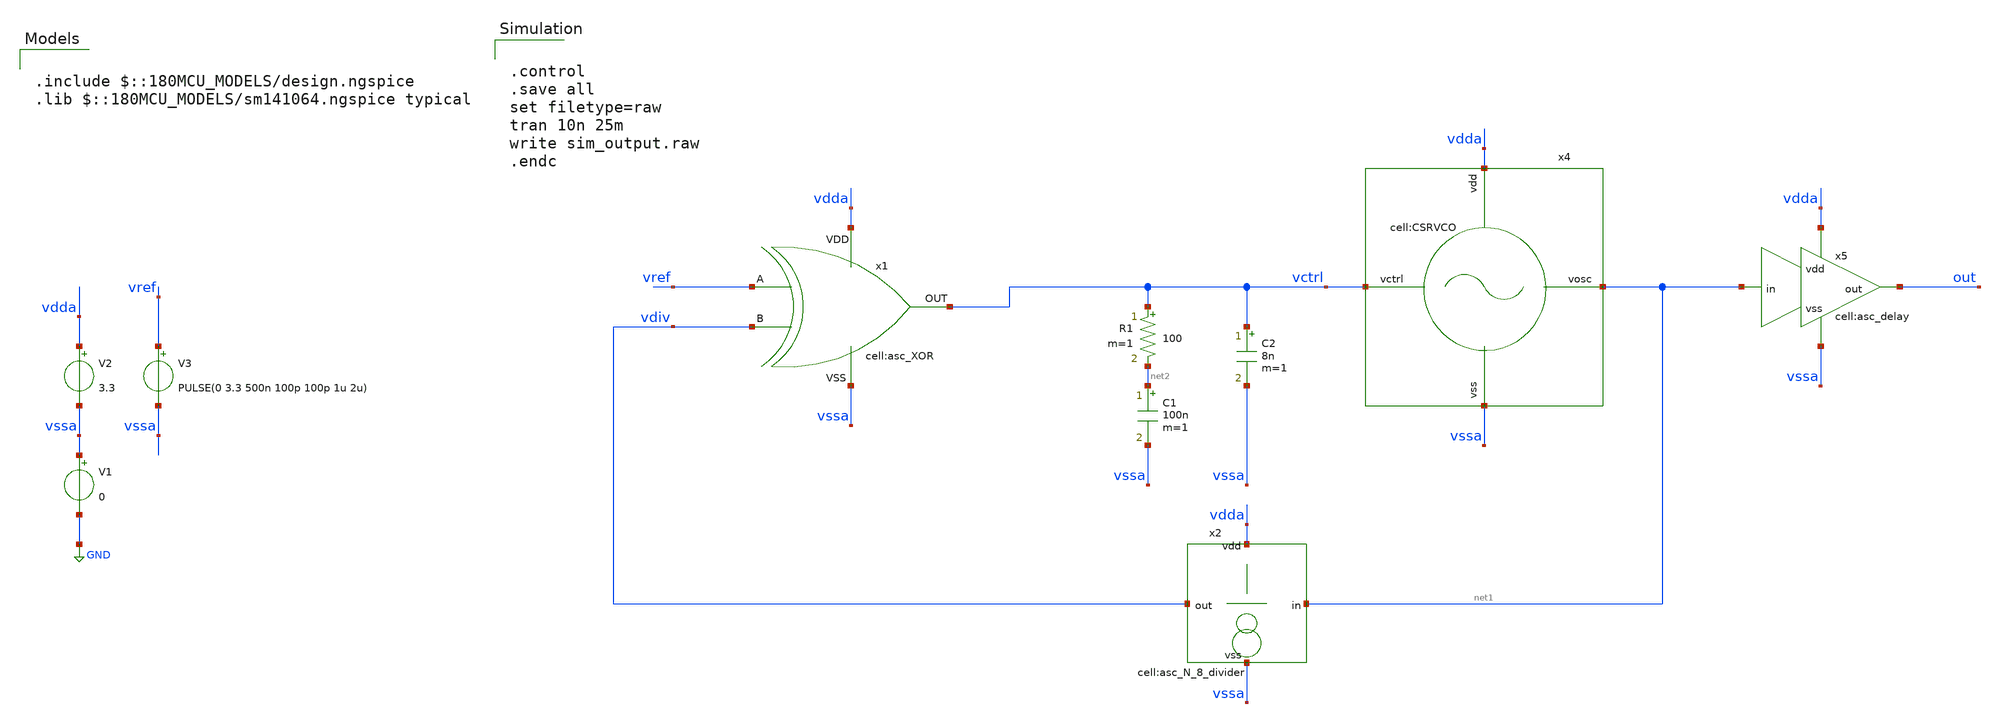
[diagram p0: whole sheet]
** sch_path: designs/libs/tb_analog/tb_xor_pll/tb_xor_pll.sch
**.subckt tb_xor_pll
V1 vssa GND 0
V2 vdda vssa 3.3
V3 vref vssa PULSE(0 3.3 500n 100p 100p 1u 2u)
x4 vctrl vdda vssa net1 CSRVCO
x5 net1 vssa out vdda asc_delay
C1 net2 vssa 100n m=1
C2 vctrl vssa 8n m=1
R1 vctrl net2 100 m=1
x1 vdda vssa vctrl vref vdiv asc_XOR
x2 net1 vdiv vdda vssa asc_N_8_divider
**** begin user architecture code

.include $::180MCU_MODELS/design.ngspice
.lib $::180MCU_MODELS/sm141064.ngspice typical



.control
.save all
set filetype=raw
tran 10n 25m
write sim_output.raw
.endc


**** end user architecture code
**.ends
.GLOBAL GND
.end
